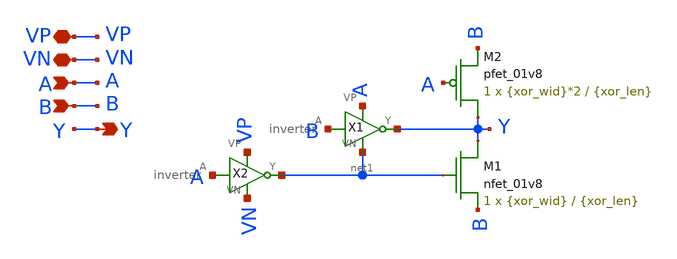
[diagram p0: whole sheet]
** sch_path: xor.sch
**.subckt xor VN VP Y A B
*.iopin VN
*.iopin VP
*.opin Y
*.ipin A
*.ipin B
X2 A net1 VP VN inverter
X1 B Y A net1 inverter
XM1 Y net1 B VN sky130_fd_pr__nfet_01v8 L={xor_len} W={xor_wid} nf=1 ad='int((nf+1)/2) * W/nf * 0.29'
+ as='int((nf+2)/2) * W/nf * 0.29' pd='2*int((nf+1)/2) * (W/nf + 0.29)' ps='2*int((nf+2)/2) * (W/nf + 0.29)'
+ nrd='0.29 / W' nrs='0.29 / W' sa=0 sb=0 sd=0 mult=1 m=1
XM2 Y A B VP sky130_fd_pr__pfet_01v8 L={xor_len} W={xor_wid}*2 nf=1 ad='int((nf+1)/2) * W/nf * 0.29'
+ as='int((nf+2)/2) * W/nf * 0.29' pd='2*int((nf+1)/2) * (W/nf + 0.29)' ps='2*int((nf+2)/2) * (W/nf + 0.29)'
+ nrd='0.29 / W' nrs='0.29 / W' sa=0 sb=0 sd=0 mult=1 m=1
**.ends

* expanding   symbol:  inverter.sym # of pins=4
** sym_path: inverter.sym
** sch_path: inverter.sch
.subckt inverter A Y VP VN
*.iopin VP
*.ipin A
*.opin Y
*.iopin VN
XM2 Y A VP VP sky130_fd_pr__pfet_01v8 L={inv_len} W={inv_wid} nf=1 ad='int((nf+1)/2) * W/nf * 0.29' as='int((nf+2)/2) * W/nf * 0.29'
+ pd='2*int((nf+1)/2) * (W/nf + 0.29)' ps='2*int((nf+2)/2) * (W/nf + 0.29)' nrd='0.29 / W' nrs='0.29 / W'
+ sa=0 sb=0 sd=0 mult=1 m=1
XM1 Y A VN VN sky130_fd_pr__nfet_01v8 L={inv_len} W={inv_wid} nf=1 ad='int((nf+1)/2) * W/nf * 0.29' as='int((nf+2)/2) * W/nf * 0.29'
+ pd='2*int((nf+1)/2) * (W/nf + 0.29)' ps='2*int((nf+2)/2) * (W/nf + 0.29)' nrd='0.29 / W' nrs='0.29 / W'
+ sa=0 sb=0 sd=0 mult=1 m=1
.ends

.end
